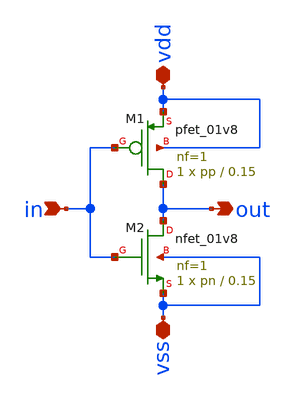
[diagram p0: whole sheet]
** sch_path: scripts/fo4/inverter.sch
**.subckt inverter out in vdd vss
*.opin out
*.ipin in
*.iopin vdd
*.iopin vss
XM1 out in vdd vdd sky130_fd_pr__pfet_01v8 L=0.15 W=pp nf=1 ad='int((nf+1)/2) * W/nf * 0.29' as='int((nf+2)/2) * W/nf * 0.29'
+ pd='2*int((nf+1)/2) * (W/nf + 0.29)' ps='2*int((nf+2)/2) * (W/nf + 0.29)' nrd='0.29 / W' nrs='0.29 / W'
+ sa=0 sb=0 sd=0 mult=1 m=1
XM2 out in vss vss sky130_fd_pr__nfet_01v8 L=0.15 W=pn nf=1 ad='int((nf+1)/2) * W/nf * 0.29' as='int((nf+2)/2) * W/nf * 0.29'
+ pd='2*int((nf+1)/2) * (W/nf + 0.29)' ps='2*int((nf+2)/2) * (W/nf + 0.29)' nrd='0.29 / W' nrs='0.29 / W'
+ sa=0 sb=0 sd=0 mult=1 m=1
**.ends
.end
